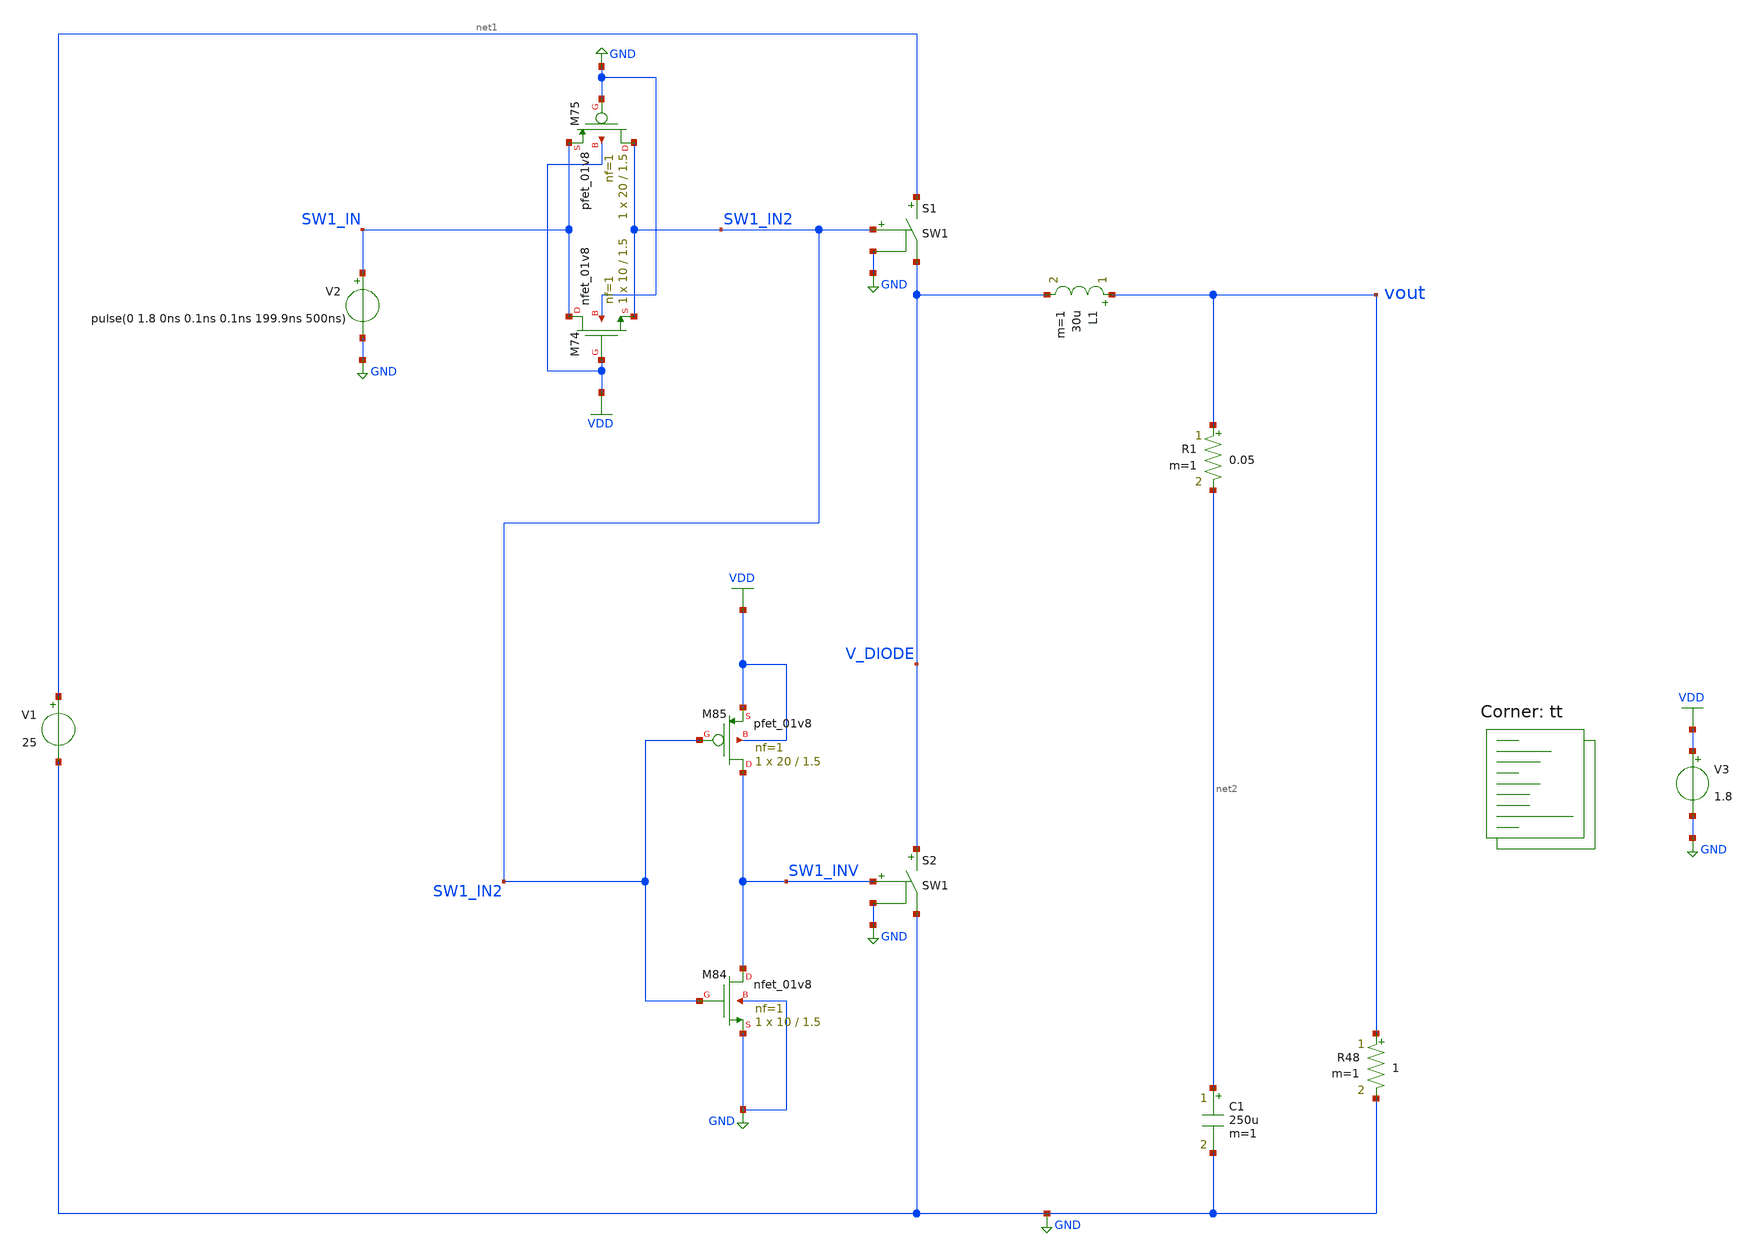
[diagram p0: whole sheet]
** sch_path: projects/ASU/EEE572/schematic/tb_buck_converter_3.sch
**.subckt tb_buck_converter_3
V1 net1 GND 25
R48 vout GND 1 m=1
L1 vout V_DIODE 30u m=1
C1 net2 GND 250u m=1
R1 vout net2 0.05 m=1
V2 SW1_IN GND pulse(0 1.8 0ns 0.1ns 0.1ns 199.9ns 500ns)
S1 net1 V_DIODE SW1_IN2 GND SW1
S2 V_DIODE GND SW1_INV GND SW1
XM84 SW1_INV SW1_IN2 GND GND sky130_fd_pr__nfet_01v8 L=1.5 W=10 nf=1 ad='int((nf+1)/2) * W/nf * 0.29'
+ as='int((nf+2)/2) * W/nf * 0.29' pd='2*int((nf+1)/2) * (W/nf + 0.29)' ps='2*int((nf+2)/2) * (W/nf + 0.29)'
+ nrd='0.29 / W' nrs='0.29 / W' sa=0 sb=0 sd=0 mult=1 m=1
XM85 SW1_INV SW1_IN2 VDD VDD sky130_fd_pr__pfet_01v8 L=1.5 W=20 nf=1 ad='int((nf+1)/2) * W/nf * 0.29'
+ as='int((nf+2)/2) * W/nf * 0.29' pd='2*int((nf+1)/2) * (W/nf + 0.29)' ps='2*int((nf+2)/2) * (W/nf + 0.29)'
+ nrd='0.29 / W' nrs='0.29 / W' sa=0 sb=0 sd=0 mult=1 m=1
V3 VDD GND 1.8
XM74 SW1_IN VDD SW1_IN2 GND sky130_fd_pr__nfet_01v8 L=1.5 W=10 nf=1 ad='int((nf+1)/2) * W/nf * 0.29'
+ as='int((nf+2)/2) * W/nf * 0.29' pd='2*int((nf+1)/2) * (W/nf + 0.29)' ps='2*int((nf+2)/2) * (W/nf + 0.29)'
+ nrd='0.29 / W' nrs='0.29 / W' sa=0 sb=0 sd=0 mult=1 m=1
XM75 SW1_IN2 GND SW1_IN VDD sky130_fd_pr__pfet_01v8 L=1.5 W=20 nf=1 ad='int((nf+1)/2) * W/nf * 0.29'
+ as='int((nf+2)/2) * W/nf * 0.29' pd='2*int((nf+1)/2) * (W/nf + 0.29)' ps='2*int((nf+2)/2) * (W/nf + 0.29)'
+ nrd='0.29 / W' nrs='0.29 / W' sa=0 sb=0 sd=0 mult=1 m=1
**** begin user architecture code



.options method=gear
.options wnflag=1
* .options savecurrents


.model D1N914 D(Is=168.1E-21 N=1 Rs=.1 Ikf=1 Xti=3 Eg=1.11 Cjo=4p M=.3333 Vj=.75 Fc=.5 Bv=100
+ Ibv=100u Tt=11.54n)


.control
  save all
  * save v(vout)
  * dc V1 0.0 2.0 0.005
  tran 10ns 3ms
  * tran 1ns 3ms
  remzerovec
  write tb_buck_converter_3.raw
  set appendwrite

.endc





.lib $::SKYWATER_MODELS/sky130.lib.spice tt
**** end user architecture code
**.ends
.GLOBAL GND
.GLOBAL VDD
**** begin user architecture code
.MODEL SW1 SW( VT=0.9 VH=0.01 RON=0.01 ROFF=10G )
**** end user architecture code
.end
